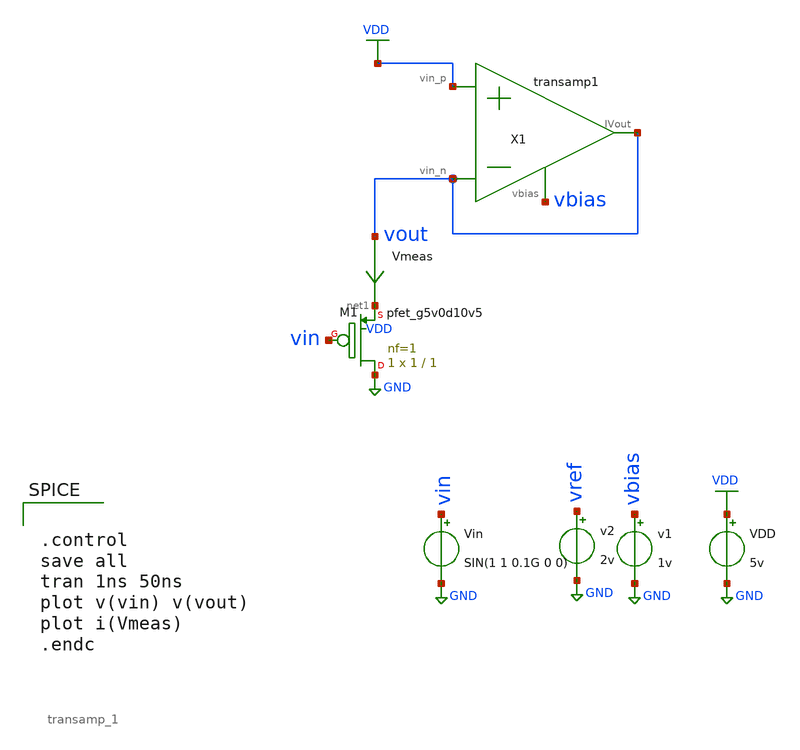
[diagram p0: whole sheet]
** sch_path: schematics/amp_tb.sch
**.subckt amp_tb
VDD VDD GND 5v
v1 vbias GND 1v
Vin vin GND SIN(1 1 0.1G 0 0)
Vmeas vout net1 0
.save i(vmeas)
v2 vref GND 2v
XM1 GND vin net1 VDD sky130_fd_pr__pfet_g5v0d10v5 L=1 W=1 nf=1 ad='int((nf+1)/2) * W/nf * 0.29' as='int((nf+2)/2) * W/nf * 0.29'
+ pd='2*int((nf+1)/2) * (W/nf + 0.29)' ps='2*int((nf+2)/2) * (W/nf + 0.29)' nrd='0.29 / W' nrs='0.29 / W'
+ sa=0 sb=0 sd=0 mult=1 m=1
X1 VDD vout vout vbias transamp_1
**** begin user architecture code


.control
save all
tran 1ns 50ns
plot v(vin) v(vout)
plot i(Vmeas)
.endc


 .lib $::SKYWATER_MODELS/models/sky130.lib.spice tt

.param mc_mm_switch=0
.param mc_pr_switch=1

**** end user architecture code
**.ends

* expanding   symbol:  /media/sf_share/final_project/transamp_1.sym # of pins=4
** sym_path: schematics/transamp_1.sym
** sch_path: schematics/transamp_1.sch
.subckt transamp_1 vin_p vin_n IVout vbias
*.opin IVout
*.ipin vin_p
*.ipin vin_n
*.ipin vbias
XM1 net1 vbias GND GND sky130_fd_pr__nfet_g5v0d10v5 L=1 W=1 nf=1 ad='int((nf+1)/2) * W/nf * 0.29' as='int((nf+2)/2) * W/nf * 0.29'
+ pd='2*int((nf+1)/2) * (W/nf + 0.29)' ps='2*int((nf+2)/2) * (W/nf + 0.29)' nrd='0.29 / W' nrs='0.29 / W'
+ sa=0 sb=0 sd=0 mult=1 m=1
XM3 net2 vin_p net1 GND sky130_fd_pr__nfet_g5v0d10v5 L=1 W=1 nf=1 ad='int((nf+1)/2) * W/nf * 0.29' as='int((nf+2)/2) * W/nf * 0.29'
+ pd='2*int((nf+1)/2) * (W/nf + 0.29)' ps='2*int((nf+2)/2) * (W/nf + 0.29)' nrd='0.29 / W' nrs='0.29 / W'
+ sa=0 sb=0 sd=0 mult=1 m=1
XM4 IVout net2 VDD VDD sky130_fd_pr__pfet_g5v0d10v5 L=1 W=1 nf=1 ad='int((nf+1)/2) * W/nf * 0.29' as='int((nf+2)/2) * W/nf * 0.29'
+ pd='2*int((nf+1)/2) * (W/nf + 0.29)' ps='2*int((nf+2)/2) * (W/nf + 0.29)' nrd='0.29 / W' nrs='0.29 / W'
+ sa=0 sb=0 sd=0 mult=1 m=1
XM2 IVout vin_n net1 GND sky130_fd_pr__nfet_g5v0d10v5 L=1 W=1 nf=1 ad='int((nf+1)/2) * W/nf * 0.29' as='int((nf+2)/2) * W/nf * 0.29'
+ pd='2*int((nf+1)/2) * (W/nf + 0.29)' ps='2*int((nf+2)/2) * (W/nf + 0.29)' nrd='0.29 / W' nrs='0.29 / W'
+ sa=0 sb=0 sd=0 mult=1 m=1
XM5 net2 net2 VDD VDD sky130_fd_pr__pfet_g5v0d10v5 L=1 W=1 nf=1 ad='int((nf+1)/2) * W/nf * 0.29' as='int((nf+2)/2) * W/nf * 0.29'
+ pd='2*int((nf+1)/2) * (W/nf + 0.29)' ps='2*int((nf+2)/2) * (W/nf + 0.29)' nrd='0.29 / W' nrs='0.29 / W'
+ sa=0 sb=0 sd=0 mult=1 m=1
.ends

.GLOBAL VDD
.GLOBAL GND
.end
